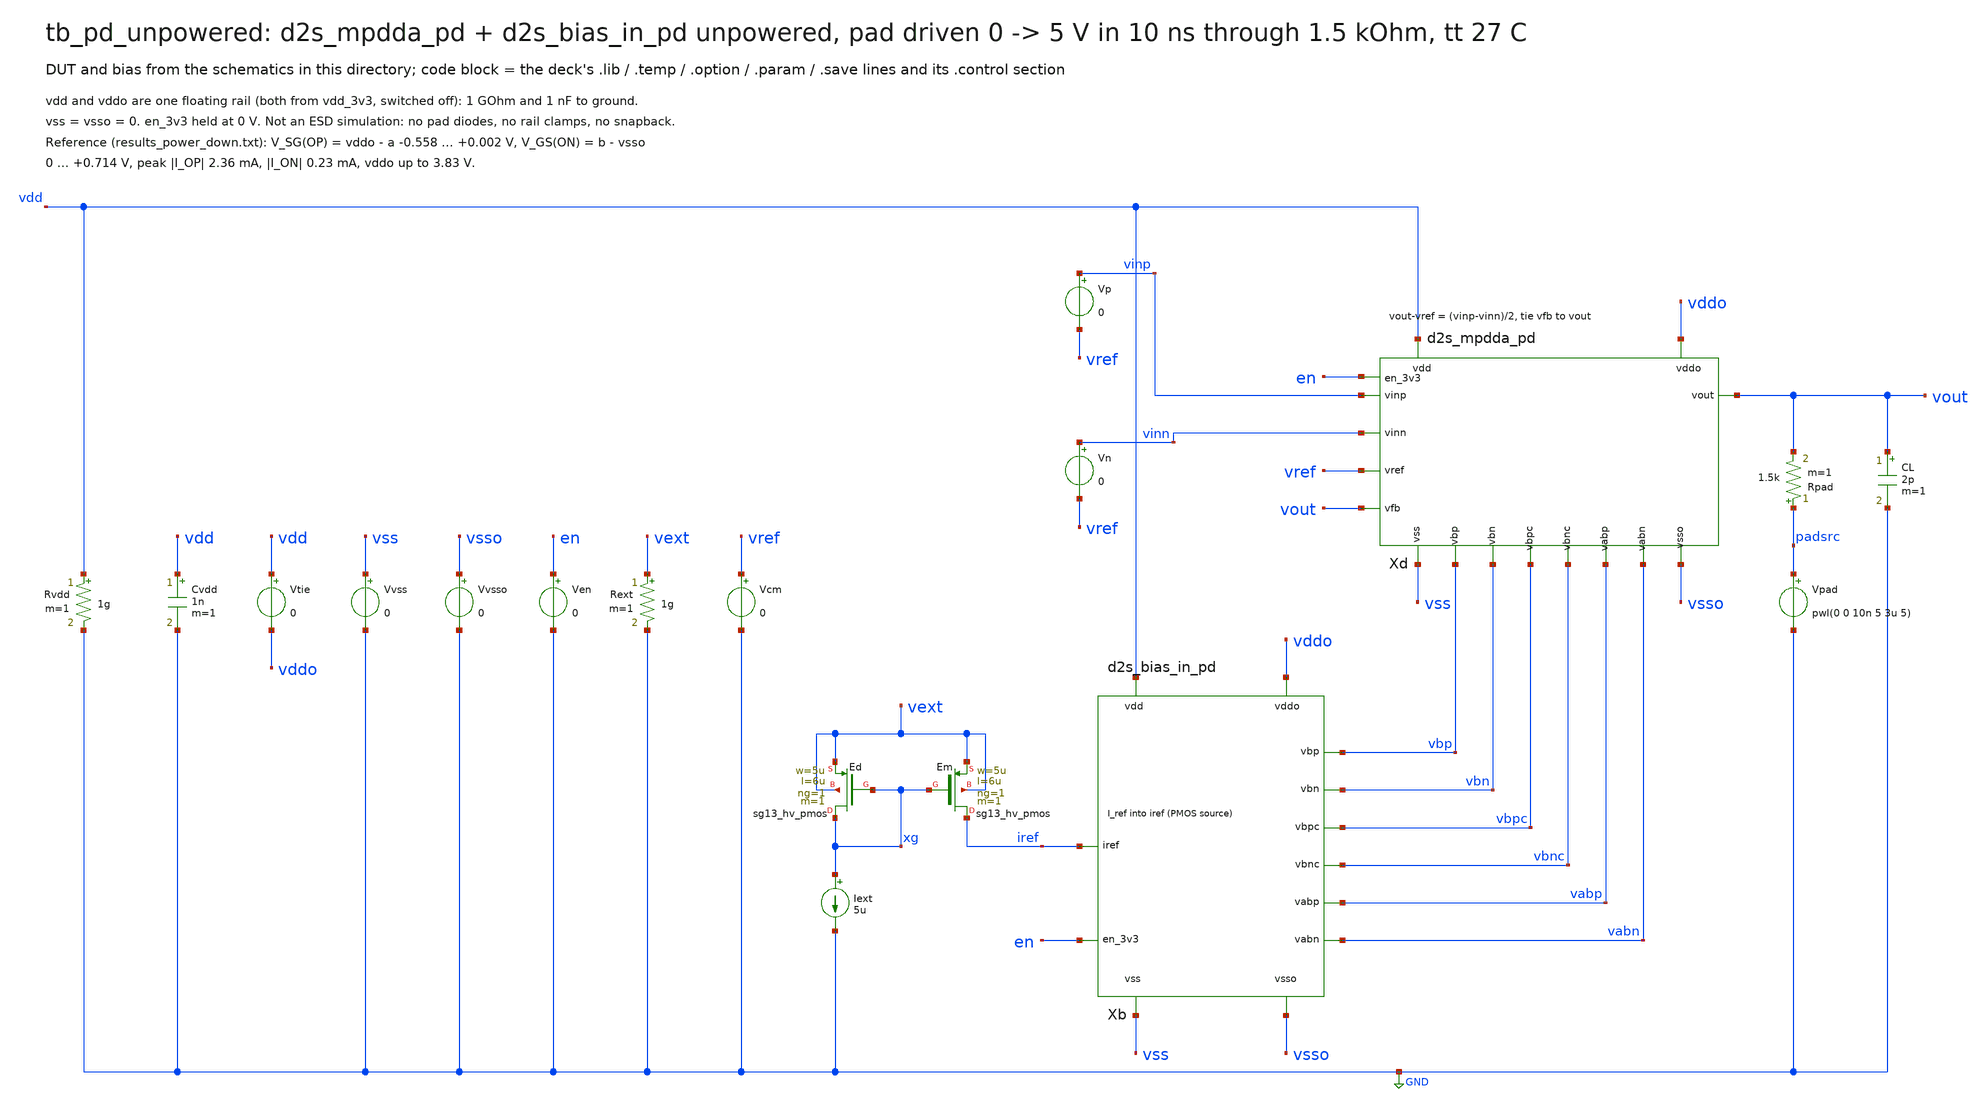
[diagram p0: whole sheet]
** sch_path: sudelbuecher/design_considerations/consolidation/reference_sheets_2026-10-20/macros/sg13cmos5l_IOPadDiff2Single/testbenches/xschem/tb_pd_unpowered.sch
**.subckt tb_pd_unpowered
Rvdd vdd GND 1g m=1
Cvdd vdd GND 1n m=1
Vtie vdd vddo 0
Vvss vss GND 0
Vvsso vsso GND 0
Ven en GND 0
Rext vext GND 1g m=1
Vcm vref GND 0
Xb vdd vss vddo vsso iref vbp vbn vbpc vbnc vabp vabn en d2s_bias_in_pd
Xd vdd vss vddo vsso vinp vinn vref vout vout vbp vbn vbpc vbnc vabp vabn en d2s_mpdda_pd
Vp vinp vref 0
Vn vinn vref 0
XEd xg xg vext vext sg13_hv_pmos w=5u l=6u ng=1 m=1 mm_ok=1
XEm iref xg vext vext sg13_hv_pmos w=5u l=6u ng=1 m=1 mm_ok=1
Iext xg GND 5u
Rpad padsrc vout 1.5k m=1
Vpad padsrc GND pwl(0 0 10n 5 3u 5)
CL vout GND 2p m=1
**** begin user architecture code

.lib cornerMOShv.lib mos_tt
.lib cornerRES.lib res_typ
.lib cornerCAP.lib cap_typ
.temp 27
.option method=gear
.save v(vout) v(xd.a) v(xd.b) v(vddo) v(xd.en_3v3_b) @n.xd.xop.nsg13_hv_pmos[ids] @n.xd.xon.nsg13_hv_nmos[ids]
.control
tran 1n 3u uic
let vsg_op = v(vddo) - v(xd.a)
let vgs_on = v(xd.b)
meas tran pmin min vsg_op
meas tran pmax max vsg_op
meas tran nmin min vgs_on
meas tran nmax max vgs_on
let ip = abs(@n.xd.xop.nsg13_hv_pmos[ids])
let inn = abs(@n.xd.xon.nsg13_hv_nmos[ids])
meas tran ipm max ip
meas tran inm max inn
meas tran vddm max v(vddo)
print pmin pmax nmin nmax ipm inm vddm
if $?batchmode = 0
  plot v(vout) v(vddo) v(xd.a) v(xd.b) v(xd.en_3v3_b)
end
.endc

**** end user architecture code
**.ends
.GLOBAL GND
.end
